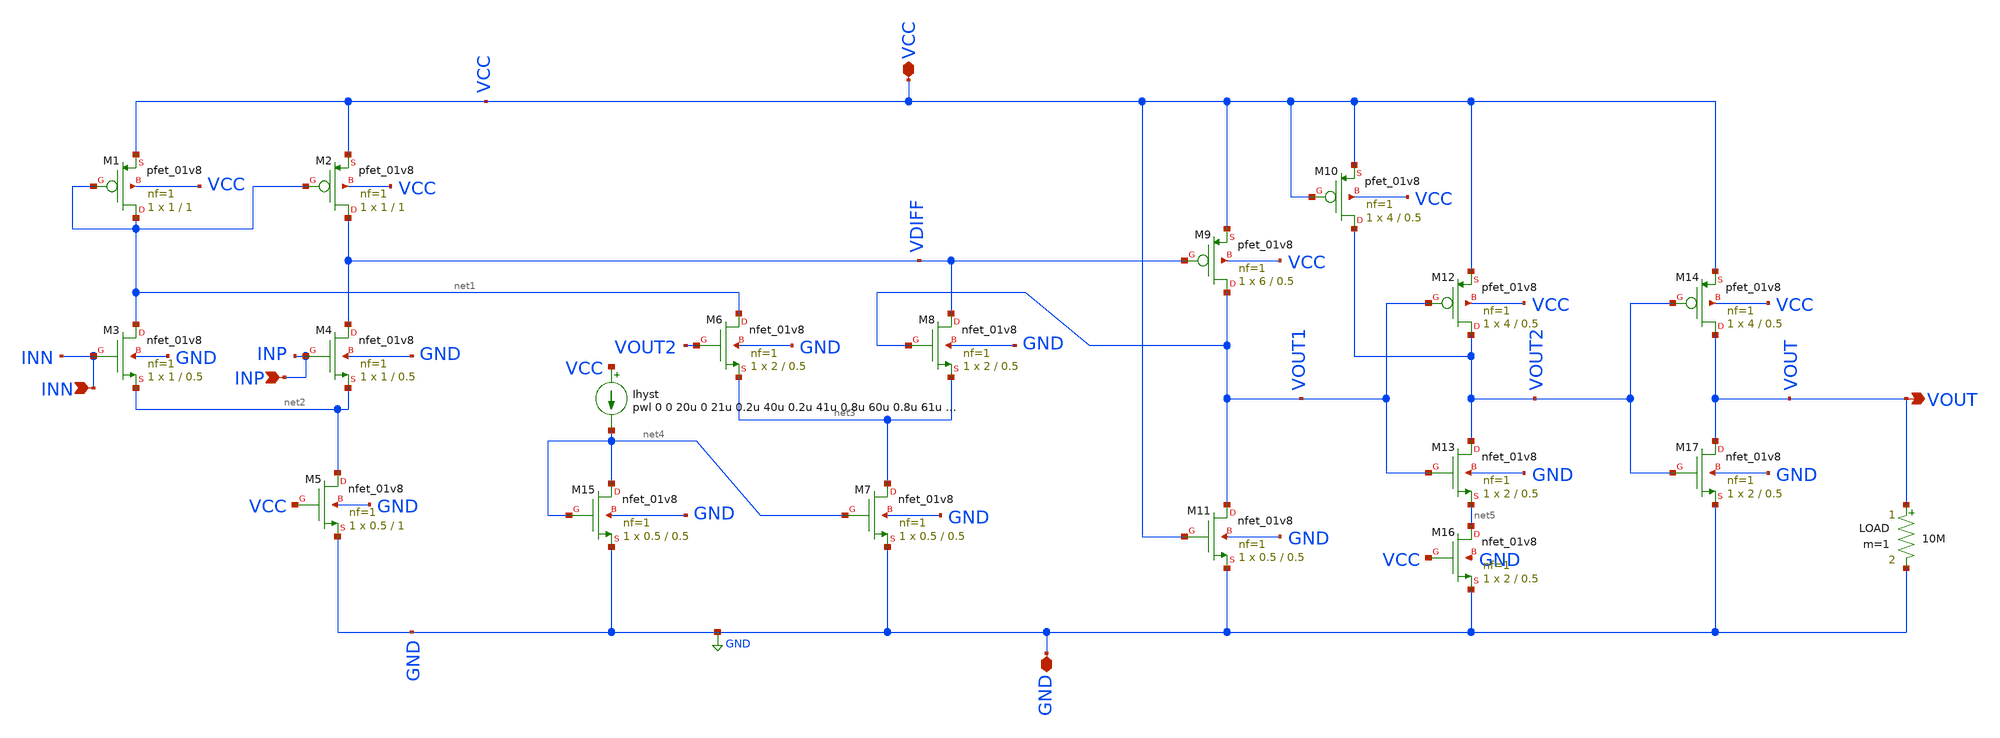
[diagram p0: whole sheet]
** sch_path: Week 4/xschem_comparator/comparator.sch
* Copyright 2020 Stefan Frederik Schippers
* Licensed under the Apache License, Version 2.0 (the "License");
* you may not use this file except in compliance with the License.
* You may obtain a copy of the License at
* https://www.apache.org/licenses/LICENSE-2.0
* Unless required by applicable law or agreed to in writing, software
* distributed under the License is distributed on an "AS IS" BASIS,
* WITHOUT WARRANTIES OR CONDITIONS OF ANY KIND, either express or implied.
* See the License for the specific language governing permissions and
* limitations under the License.
**.subckt comparator VCC GND VOUT INP INN
*.iopin VCC
*.iopin GND
*.opin VOUT
*.ipin INP
*.ipin INN
Ihyst VCC net4 pwl 0 0 20u 0 21u 0.2u 40u 0.2u 41u 0.8u 60u 0.8u 61u 10u 100u 10u
LOAD VOUT GND 10M m=1
XM1 net1 net1 VCC VCC sky130_fd_pr__pfet_01v8 L=1 W=1 nf=1 ad='int((nf+1)/2) * W/nf * 0.29' as='int((nf+2)/2) * W/nf * 0.29'
+ pd='2*int((nf+1)/2) * (W/nf + 0.29)' ps='2*int((nf+2)/2) * (W/nf + 0.29)' nrd='0.29 / W' nrs='0.29 / W'
+ sa=0 sb=0 sd=0 mult=1 m=1
XM2 VDIFF net1 VCC VCC sky130_fd_pr__pfet_01v8 L=1 W=1 nf=1 ad='int((nf+1)/2) * W/nf * 0.29' as='int((nf+2)/2) * W/nf * 0.29'
+ pd='2*int((nf+1)/2) * (W/nf + 0.29)' ps='2*int((nf+2)/2) * (W/nf + 0.29)' nrd='0.29 / W' nrs='0.29 / W'
+ sa=0 sb=0 sd=0 mult=1 m=1
XM9 VOUT1 VDIFF VCC VCC sky130_fd_pr__pfet_01v8 L=0.5 W=6 nf=1 ad='int((nf+1)/2) * W/nf * 0.29' as='int((nf+2)/2) * W/nf * 0.29'
+ pd='2*int((nf+1)/2) * (W/nf + 0.29)' ps='2*int((nf+2)/2) * (W/nf + 0.29)' nrd='0.29 / W' nrs='0.29 / W'
+ sa=0 sb=0 sd=0 mult=1 m=1
XM10 VOUT2 VCC VCC VCC sky130_fd_pr__pfet_01v8 L=0.5 W=4 nf=1 ad='int((nf+1)/2) * W/nf * 0.29' as='int((nf+2)/2) * W/nf * 0.29'
+ pd='2*int((nf+1)/2) * (W/nf + 0.29)' ps='2*int((nf+2)/2) * (W/nf + 0.29)' nrd='0.29 / W' nrs='0.29 / W'
+ sa=0 sb=0 sd=0 mult=1 m=1
XM12 VOUT2 VOUT1 VCC VCC sky130_fd_pr__pfet_01v8 L=0.5 W=4 nf=1 ad='int((nf+1)/2) * W/nf * 0.29' as='int((nf+2)/2) * W/nf * 0.29'
+ pd='2*int((nf+1)/2) * (W/nf + 0.29)' ps='2*int((nf+2)/2) * (W/nf + 0.29)' nrd='0.29 / W' nrs='0.29 / W'
+ sa=0 sb=0 sd=0 mult=1 m=1
XM14 VOUT VOUT2 VCC VCC sky130_fd_pr__pfet_01v8 L=0.5 W=4 nf=1 ad='int((nf+1)/2) * W/nf * 0.29' as='int((nf+2)/2) * W/nf * 0.29'
+ pd='2*int((nf+1)/2) * (W/nf + 0.29)' ps='2*int((nf+2)/2) * (W/nf + 0.29)' nrd='0.29 / W' nrs='0.29 / W'
+ sa=0 sb=0 sd=0 mult=1 m=1
XM3 net1 INN net2 GND sky130_fd_pr__nfet_01v8 L=0.5 W=1 nf=1 ad='int((nf+1)/2) * W/nf * 0.29' as='int((nf+2)/2) * W/nf * 0.29'
+ pd='2*int((nf+1)/2) * (W/nf + 0.29)' ps='2*int((nf+2)/2) * (W/nf + 0.29)' nrd='0.29 / W' nrs='0.29 / W'
+ sa=0 sb=0 sd=0 mult=1 m=1
XM4 VDIFF INP net2 GND sky130_fd_pr__nfet_01v8 L=0.5 W=1 nf=1 ad='int((nf+1)/2) * W/nf * 0.29' as='int((nf+2)/2) * W/nf * 0.29'
+ pd='2*int((nf+1)/2) * (W/nf + 0.29)' ps='2*int((nf+2)/2) * (W/nf + 0.29)' nrd='0.29 / W' nrs='0.29 / W'
+ sa=0 sb=0 sd=0 mult=1 m=1
XM5 net2 VCC GND GND sky130_fd_pr__nfet_01v8 L=1 W=0.5 nf=1 ad='int((nf+1)/2) * W/nf * 0.29' as='int((nf+2)/2) * W/nf * 0.29'
+ pd='2*int((nf+1)/2) * (W/nf + 0.29)' ps='2*int((nf+2)/2) * (W/nf + 0.29)' nrd='0.29 / W' nrs='0.29 / W'
+ sa=0 sb=0 sd=0 mult=1 m=1
XM15 net4 net4 GND GND sky130_fd_pr__nfet_01v8 L=0.5 W=0.5 nf=1 ad='int((nf+1)/2) * W/nf * 0.29' as='int((nf+2)/2) * W/nf * 0.29'
+ pd='2*int((nf+1)/2) * (W/nf + 0.29)' ps='2*int((nf+2)/2) * (W/nf + 0.29)' nrd='0.29 / W' nrs='0.29 / W'
+ sa=0 sb=0 sd=0 mult=1 m=1
XM7 net3 net4 GND GND sky130_fd_pr__nfet_01v8 L=0.5 W=0.5 nf=1 ad='int((nf+1)/2) * W/nf * 0.29' as='int((nf+2)/2) * W/nf * 0.29'
+ pd='2*int((nf+1)/2) * (W/nf + 0.29)' ps='2*int((nf+2)/2) * (W/nf + 0.29)' nrd='0.29 / W' nrs='0.29 / W'
+ sa=0 sb=0 sd=0 mult=1 m=1
XM11 VOUT1 VCC GND GND sky130_fd_pr__nfet_01v8 L=0.5 W=0.5 nf=1 ad='int((nf+1)/2) * W/nf * 0.29' as='int((nf+2)/2) * W/nf * 0.29'
+ pd='2*int((nf+1)/2) * (W/nf + 0.29)' ps='2*int((nf+2)/2) * (W/nf + 0.29)' nrd='0.29 / W' nrs='0.29 / W'
+ sa=0 sb=0 sd=0 mult=1 m=1
XM6 net1 VOUT2 net3 GND sky130_fd_pr__nfet_01v8 L=0.5 W=2 nf=1 ad='int((nf+1)/2) * W/nf * 0.29' as='int((nf+2)/2) * W/nf * 0.29'
+ pd='2*int((nf+1)/2) * (W/nf + 0.29)' ps='2*int((nf+2)/2) * (W/nf + 0.29)' nrd='0.29 / W' nrs='0.29 / W'
+ sa=0 sb=0 sd=0 mult=1 m=1
XM8 VDIFF VOUT1 net3 GND sky130_fd_pr__nfet_01v8 L=0.5 W=2 nf=1 ad='int((nf+1)/2) * W/nf * 0.29' as='int((nf+2)/2) * W/nf * 0.29'
+ pd='2*int((nf+1)/2) * (W/nf + 0.29)' ps='2*int((nf+2)/2) * (W/nf + 0.29)' nrd='0.29 / W' nrs='0.29 / W'
+ sa=0 sb=0 sd=0 mult=1 m=1
XM13 VOUT2 VOUT1 net5 GND sky130_fd_pr__nfet_01v8 L=0.5 W=2 nf=1 ad='int((nf+1)/2) * W/nf * 0.29' as='int((nf+2)/2) * W/nf * 0.29'
+ pd='2*int((nf+1)/2) * (W/nf + 0.29)' ps='2*int((nf+2)/2) * (W/nf + 0.29)' nrd='0.29 / W' nrs='0.29 / W'
+ sa=0 sb=0 sd=0 mult=1 m=1
XM16 net5 VCC GND GND sky130_fd_pr__nfet_01v8 L=0.5 W=2 nf=1 ad='int((nf+1)/2) * W/nf * 0.29' as='int((nf+2)/2) * W/nf * 0.29'
+ pd='2*int((nf+1)/2) * (W/nf + 0.29)' ps='2*int((nf+2)/2) * (W/nf + 0.29)' nrd='0.29 / W' nrs='0.29 / W'
+ sa=0 sb=0 sd=0 mult=1 m=1
XM17 VOUT VOUT2 GND GND sky130_fd_pr__nfet_01v8 L=0.5 W=2 nf=1 ad='int((nf+1)/2) * W/nf * 0.29' as='int((nf+2)/2) * W/nf * 0.29'
+ pd='2*int((nf+1)/2) * (W/nf + 0.29)' ps='2*int((nf+2)/2) * (W/nf + 0.29)' nrd='0.29 / W' nrs='0.29 / W'
+ sa=0 sb=0 sd=0 mult=1 m=1
**.ends
.GLOBAL GND
.end
